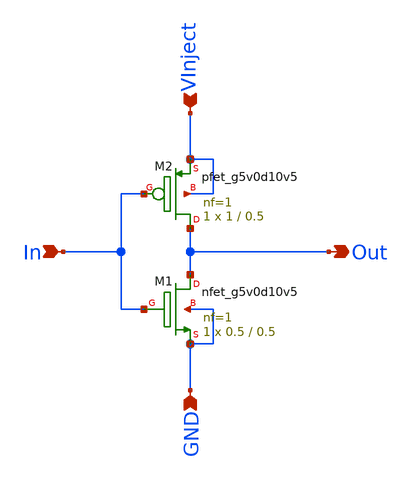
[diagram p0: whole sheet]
** sch_path: sky130_cells/IndirectVMM_DrainSwcs/Inverter.sch
**.subckt Inverter In VInject GND Out
*.ipin In
*.ipin VInject
*.ipin GND
*.opin Out
XM1 Out In GND GND sky130_fd_pr__nfet_g5v0d10v5 L=0.5 W=0.5 nf=1 ad='int((1 + 1)/2) * 0.5 / 1 * 0.29'
+ as='int((1 + 2)/2) * 0.5 / 1 * 0.29' pd='2*int((1 + 1)/2) * (0.5 / 1 + 0.29)' ps='2*int((1 + 2)/2) * (0.5 / 1 + 0.29)'
+ nrd='0.29 / 0.5 ' nrs='0.29 / 0.5 ' sa=0 sb=0 sd=0 mult=1 m=1
XM2 Out In VInject VInject sky130_fd_pr__pfet_g5v0d10v5 L=0.5 W=1 nf=1 ad='int((1 + 1)/2) * 1 / 1 * 0.29'
+ as='int((1 + 2)/2) * 1 / 1 * 0.29' pd='2*int((1 + 1)/2) * (1 / 1 + 0.29)' ps='2*int((1 + 2)/2) * (1 / 1 + 0.29)'
+ nrd='0.29 / 1 ' nrs='0.29 / 1 ' sa=0 sb=0 sd=0 mult=1 m=1
**.ends
.end
